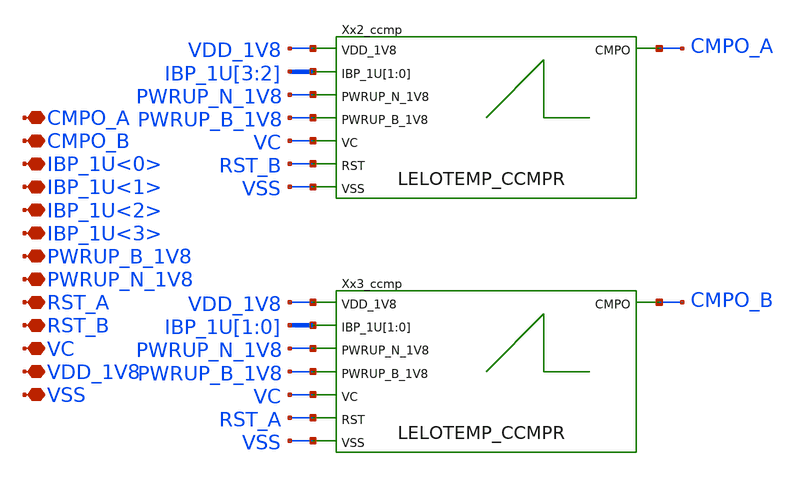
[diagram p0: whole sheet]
** sch_path: design/LELO_TEMP_SKY130A/LELO_TEMP_CCMP.sch
**.subckt LELO_TEMP_CCMP CMPO_A CMPO_B IBP_1U<0> IBP_1U<1> IBP_1U<2> IBP_1U<3> PWRUP_B_1V8
*+ PWRUP_N_1V8 RST_A RST_B VC VDD_1V8 VSS
*.iopin CMPO_A
*.iopin CMPO_B
*.iopin IBP_1U<0>
*.iopin IBP_1U<1>
*.iopin IBP_1U<2>
*.iopin IBP_1U<3>
*.iopin PWRUP_B_1V8
*.iopin PWRUP_N_1V8
*.iopin RST_A
*.iopin RST_B
*.iopin VC
*.iopin VDD_1V8
*.iopin VSS
Xx2_ccmp IBP_1U[3] IBP_1U[2] VDD_1V8 PWRUP_N_1V8 PWRUP_B_1V8 CMPO_A VC RST_B VSS LELOTEMP_CCMPR
Xx3_ccmp IBP_1U[1] IBP_1U[0] VDD_1V8 PWRUP_N_1V8 PWRUP_B_1V8 CMPO_B VC RST_A VSS LELOTEMP_CCMPR
**.ends
.end
